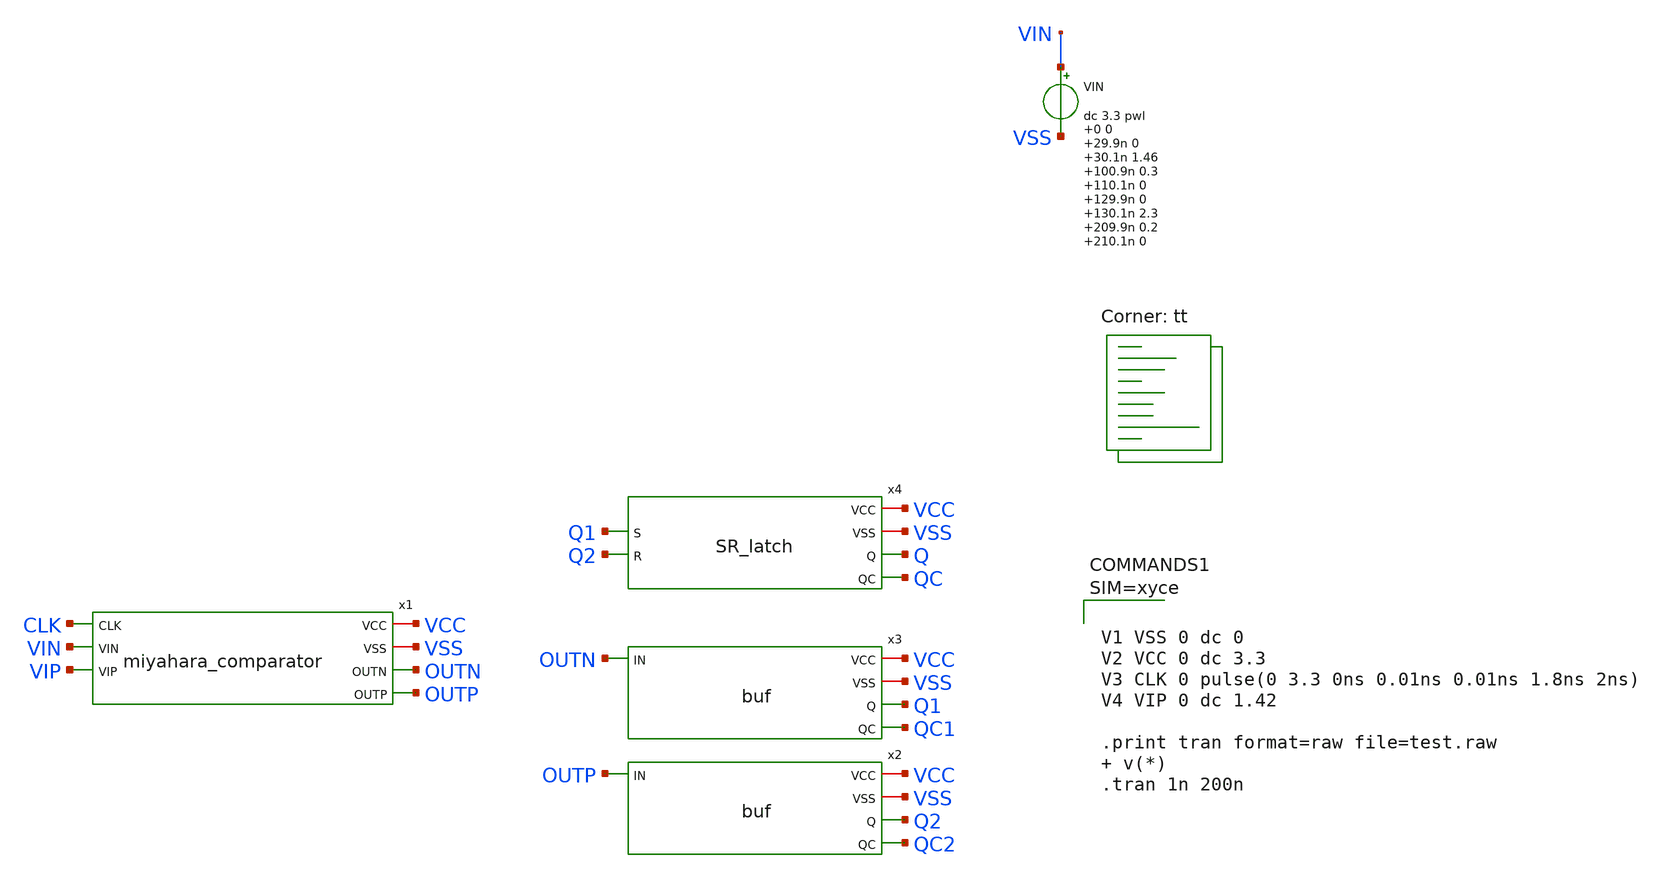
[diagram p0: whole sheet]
** sch_path: Comparator/schematic/Edge_pursuit_comparator/miyahara_comparator_testbench.sch
**.subckt miyahara_comparator_testbench
x1 VCC VSS CLK VIN VIP OUTN OUTP miyahara_comparator
VIN VIN VSS dc 3.3 pwl 0 0 29.9n 0 30.1n 1.46 100.9n 0.3 110.1n 0 129.9n 0 130.1n 2.3 209.9n 0.2
+ 210.1n 0
x3 VCC VSS OUTN Q1 QC1 buf
x2 VCC VSS OUTP Q2 QC2 buf
x4 VCC VSS Q1 Q2 Q QC SR_latch
**** begin user architecture code
.lib $::SKYWATER_MODELS/sky130.lib.spice tt



**** end user architecture code
**.ends
.end
